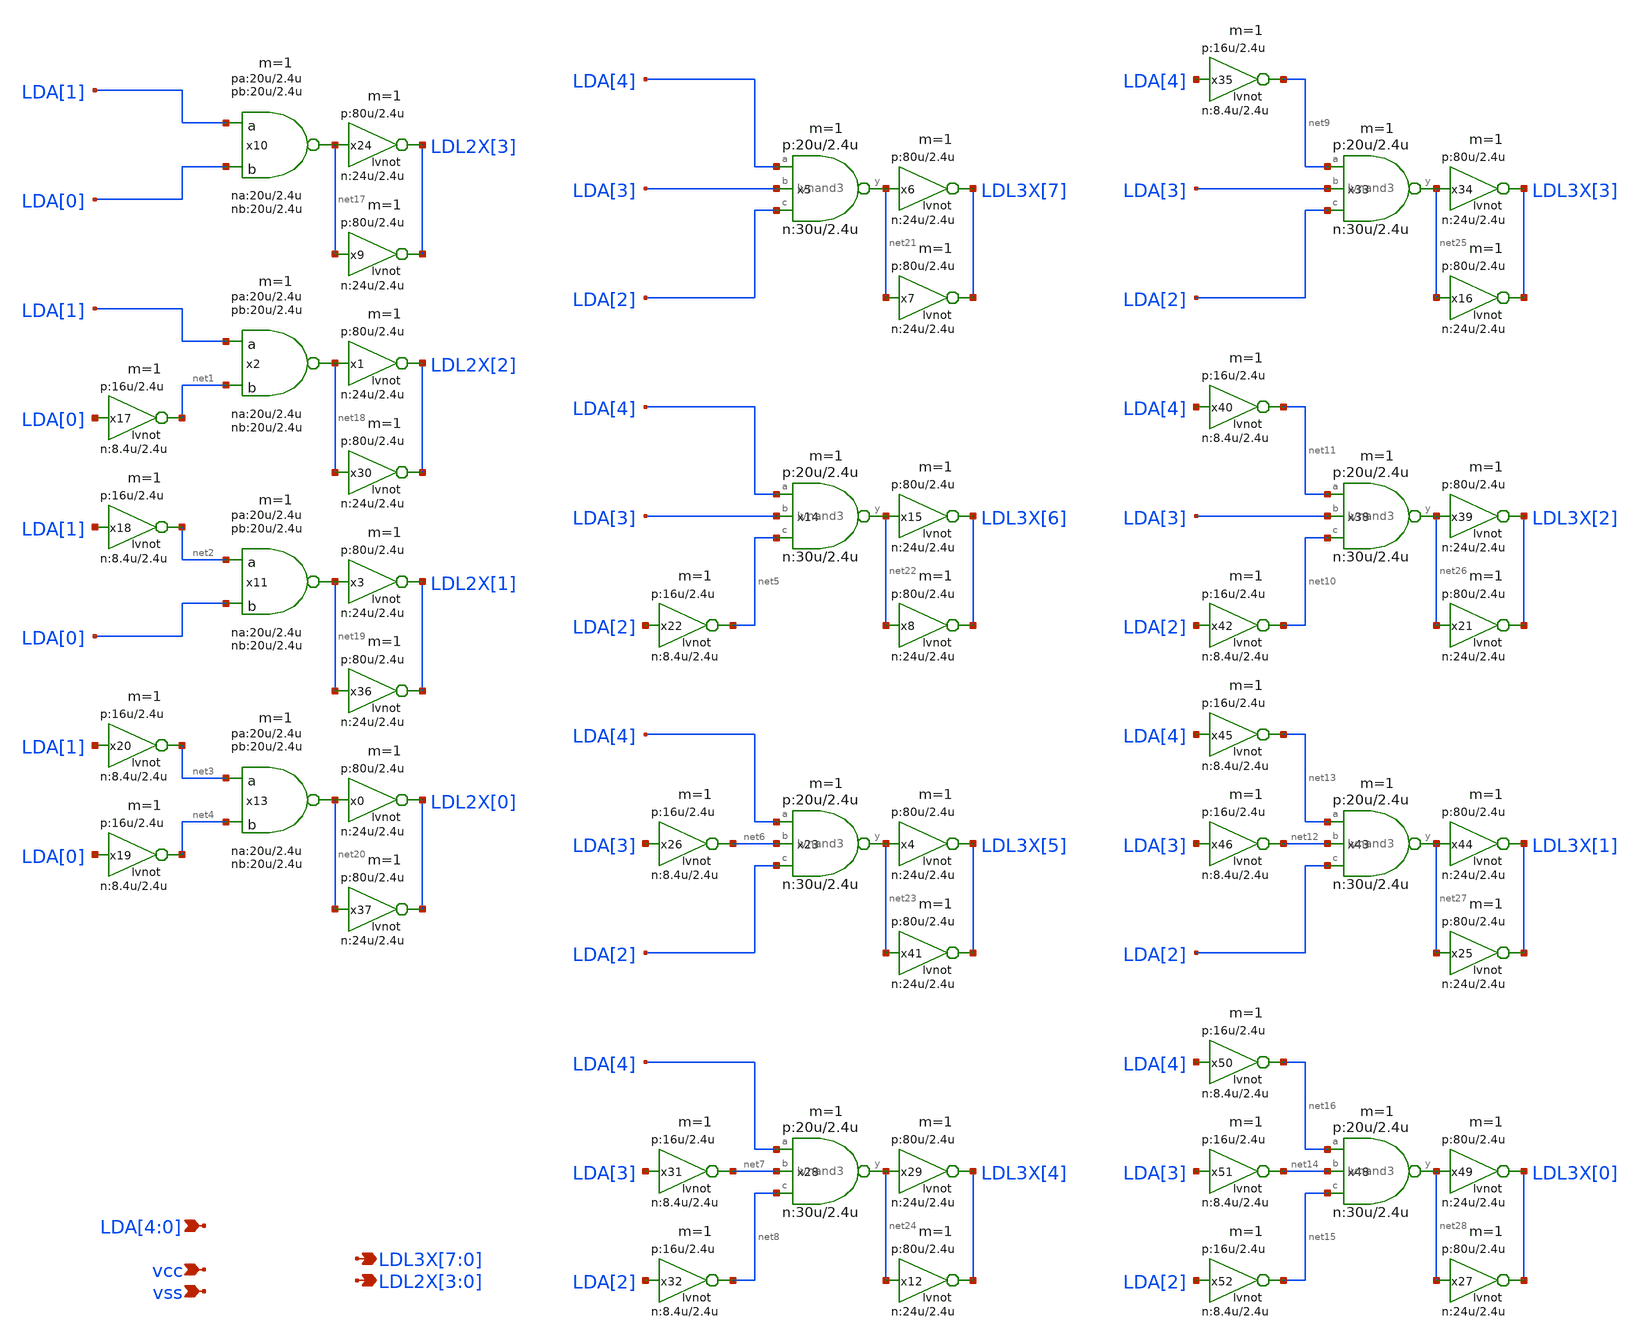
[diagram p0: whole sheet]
** sch_path: xschem-src/xschem_library/rom8k/rom2_predec4.sch
* Copyright (C) 1998-2026 Stefan Frederik Schippers
* This program is free software; you can redistribute it and/or modify
* it under the terms of the GNU General Public License as published by
* the Free Software Foundation; either version 2 of the License, or
* (at your option) any later version.
* This program is distributed in the hope that it will be useful,
* but WITHOUT ANY WARRANTY; without even the implied warranty of
* MERCHANTABILITY or FITNESS FOR A PARTICULAR PURPOSE.  See the
* GNU General Public License for more details.
* You should have received a copy of the GNU General Public License
* along with this program; if not, write to the Free Software
**.subckt rom2_predec4 LDA[4],LDA[3],LDA[2],LDA[1],LDA[0] vcc vss
*+ LDL2X[3],LDL2X[2],LDL2X[1],LDL2X[0] LDL3X[7],LDL3X[6],LDL3X[5],LDL3X[4],LDL3X[3],LDL3X[2],LDL3X[1],LDL3X[0]
*.ipin LDA[4],LDA[3],LDA[2],LDA[1],LDA[0]
*.ipin vcc
*.ipin vss
*.opin LDL2X[3],LDL2X[2],LDL2X[1],LDL2X[0]
*.opin LDL3X[7],LDL3X[6],LDL3X[5],LDL3X[4],LDL3X[3],LDL3X[2],LDL3X[1],LDL3X[0]
x10 net17 LDA[1] LDA[0] vcc vss lvnand2 wna=20u lna=2.4u wpa=20u lpa=2.4u wnb=20u lnb=2.4u wpb=20u
+ lpb=2.4u m=1
x2 net18 LDA[1] net1 vcc vss lvnand2 wna=20u lna=2.4u wpa=20u lpa=2.4u wnb=20u lnb=2.4u wpb=20u
+ lpb=2.4u m=1
x11 net19 net2 LDA[0] vcc vss lvnand2 wna=20u lna=2.4u wpa=20u lpa=2.4u wnb=20u lnb=2.4u wpb=20u
+ lpb=2.4u m=1
x13 net20 net3 net4 vcc vss lvnand2 wna=20u lna=2.4u wpa=20u lpa=2.4u wnb=20u lnb=2.4u wpb=20u
+ lpb=2.4u m=1
x17 net1 LDA[0] vcc vss lvnot wn=8.4u lln=2.4u wp=16u lp=2.4u m=1
x18 net2 LDA[1] vcc vss lvnot wn=8.4u lln=2.4u wp=16u lp=2.4u m=1
x19 net4 LDA[0] vcc vss lvnot wn=8.4u lln=2.4u wp=16u lp=2.4u m=1
x20 net3 LDA[1] vcc vss lvnot wn=8.4u lln=2.4u wp=16u lp=2.4u m=1
x5 net21 LDA[4] LDA[3] LDA[2] vcc vss lvnand3 wn=30u lln=2.4u wp=20u lp=2.4u m=1
x6 LDL3X[7] net21 vcc vss lvnot wn=24u lln=2.4u wp=80u lp=2.4u m=1
x14 net22 LDA[4] LDA[3] net5 vcc vss lvnand3 wn=30u lln=2.4u wp=20u lp=2.4u m=1
x15 LDL3X[6] net22 vcc vss lvnot wn=24u lln=2.4u wp=80u lp=2.4u m=1
x22 net5 LDA[2] vcc vss lvnot wn=8.4u lln=2.4u wp=16u lp=2.4u m=1
x23 net23 LDA[4] net6 LDA[2] vcc vss lvnand3 wn=30u lln=2.4u wp=20u lp=2.4u m=1
x24 LDL2X[3] net17 vcc vss lvnot wn=24u lln=2.4u wp=80u lp=2.4u m=1
x26 net6 LDA[3] vcc vss lvnot wn=8.4u lln=2.4u wp=16u lp=2.4u m=1
x28 net24 LDA[4] net7 net8 vcc vss lvnand3 wn=30u lln=2.4u wp=20u lp=2.4u m=1
x29 LDL3X[4] net24 vcc vss lvnot wn=24u lln=2.4u wp=80u lp=2.4u m=1
x31 net7 LDA[3] vcc vss lvnot wn=8.4u lln=2.4u wp=16u lp=2.4u m=1
x32 net8 LDA[2] vcc vss lvnot wn=8.4u lln=2.4u wp=16u lp=2.4u m=1
x33 net25 net9 LDA[3] LDA[2] vcc vss lvnand3 wn=30u lln=2.4u wp=20u lp=2.4u m=1
x34 LDL3X[3] net25 vcc vss lvnot wn=24u lln=2.4u wp=80u lp=2.4u m=1
x35 net9 LDA[4] vcc vss lvnot wn=8.4u lln=2.4u wp=16u lp=2.4u m=1
x38 net26 net11 LDA[3] net10 vcc vss lvnand3 wn=30u lln=2.4u wp=20u lp=2.4u m=1
x39 LDL3X[2] net26 vcc vss lvnot wn=24u lln=2.4u wp=80u lp=2.4u m=1
x40 net11 LDA[4] vcc vss lvnot wn=8.4u lln=2.4u wp=16u lp=2.4u m=1
x42 net10 LDA[2] vcc vss lvnot wn=8.4u lln=2.4u wp=16u lp=2.4u m=1
x43 net27 net13 net12 LDA[2] vcc vss lvnand3 wn=30u lln=2.4u wp=20u lp=2.4u m=1
x44 LDL3X[1] net27 vcc vss lvnot wn=24u lln=2.4u wp=80u lp=2.4u m=1
x45 net13 LDA[4] vcc vss lvnot wn=8.4u lln=2.4u wp=16u lp=2.4u m=1
x46 net12 LDA[3] vcc vss lvnot wn=8.4u lln=2.4u wp=16u lp=2.4u m=1
x48 net28 net16 net14 net15 vcc vss lvnand3 wn=30u lln=2.4u wp=20u lp=2.4u m=1
x49 LDL3X[0] net28 vcc vss lvnot wn=24u lln=2.4u wp=80u lp=2.4u m=1
x50 net16 LDA[4] vcc vss lvnot wn=8.4u lln=2.4u wp=16u lp=2.4u m=1
x51 net14 LDA[3] vcc vss lvnot wn=8.4u lln=2.4u wp=16u lp=2.4u m=1
x52 net15 LDA[2] vcc vss lvnot wn=8.4u lln=2.4u wp=16u lp=2.4u m=1
x1 LDL2X[2] net18 vcc vss lvnot wn=24u lln=2.4u wp=80u lp=2.4u m=1
x3 LDL2X[1] net19 vcc vss lvnot wn=24u lln=2.4u wp=80u lp=2.4u m=1
x0 LDL2X[0] net20 vcc vss lvnot wn=24u lln=2.4u wp=80u lp=2.4u m=1
x4 LDL3X[5] net23 vcc vss lvnot wn=24u lln=2.4u wp=80u lp=2.4u m=1
x7 LDL3X[7] net21 vcc vss lvnot wn=24u lln=2.4u wp=80u lp=2.4u m=1
x8 LDL3X[6] net22 vcc vss lvnot wn=24u lln=2.4u wp=80u lp=2.4u m=1
x9 LDL2X[3] net17 vcc vss lvnot wn=24u lln=2.4u wp=80u lp=2.4u m=1
x12 LDL3X[4] net24 vcc vss lvnot wn=24u lln=2.4u wp=80u lp=2.4u m=1
x16 LDL3X[3] net25 vcc vss lvnot wn=24u lln=2.4u wp=80u lp=2.4u m=1
x21 LDL3X[2] net26 vcc vss lvnot wn=24u lln=2.4u wp=80u lp=2.4u m=1
x25 LDL3X[1] net27 vcc vss lvnot wn=24u lln=2.4u wp=80u lp=2.4u m=1
x27 LDL3X[0] net28 vcc vss lvnot wn=24u lln=2.4u wp=80u lp=2.4u m=1
x30 LDL2X[2] net18 vcc vss lvnot wn=24u lln=2.4u wp=80u lp=2.4u m=1
x36 LDL2X[1] net19 vcc vss lvnot wn=24u lln=2.4u wp=80u lp=2.4u m=1
x37 LDL2X[0] net20 vcc vss lvnot wn=24u lln=2.4u wp=80u lp=2.4u m=1
x41 LDL3X[5] net23 vcc vss lvnot wn=24u lln=2.4u wp=80u lp=2.4u m=1
**.ends

* expanding   symbol:  lvnand2.sym # of pins=3
** sym_path: xschem-src/xschem_library/rom8k/lvnand2.sym
** sch_path: xschem-src/xschem_library/rom8k/lvnand2.sch
.subckt lvnand2 y a b VCCPIN VSSPIN     wna=8u lna=1.2u wpa=10u lpa=1.2u  wnb=8u lnb=1.2u wpb=10u
+ lpb=1.2u
*.opin y
*.ipin a
*.ipin b
m2 y a VCCPIN VCCPIN cmosp w=wpa l=lpa ad='wpa *4.6u' as='wpa *4.6u' pd='wpa *2+9.2u' ps='wpa *2+9.2u'
+ m=1
m1 y b VCCPIN VCCPIN cmosp w=wpb l=lpb ad='wpb *4.6u' as='wpb *4.6u' pd='wpb *2+9.2u' ps='wpb *2+9.2u'
+ m=1
m3 y a net1 VSSPIN cmosn w=wna l=lna ad='wna *4.3u' as='wna *4.3u' pd='wna *2+8.6u' ps='wna *2+8.6u'
+ m=1
m4 net1 b VSSPIN VSSPIN cmosn w=wnb l=lnb ad='wnb *4.3u' as='wnb *4.3u' pd='wnb *2+8.6u' ps='wnb *2+8.6u'
+ m=1
.ends


* expanding   symbol:  lvnot.sym # of pins=2
** sym_path: xschem-src/xschem_library/rom8k/lvnot.sym
** sch_path: xschem-src/xschem_library/rom8k/lvnot.sch
.subckt lvnot y a VCCPIN VSSPIN     wn=10u lln=1.2u wp=10u lp=1.2u
*.opin y
*.ipin a
m2 DP a VCCPIN VCCPIN cmosp w=wp l=lp ad='wp *4.6u' as='wp *4.6u' pd='wp *2+9.2u' ps='wp *2+9.2u' m=1
m1 DN a VSSPIN VSSPIN cmosn w=wn l=lln ad='wn *4.3u' as='wn *4.3u' pd='wn *2+8.6u' ps='wn *2+8.6u' m=1
Vmeas DP y 0
.save i(vmeas)
Vmeas1 y DN 0
.save i(vmeas1)
.save v(dp)
.save v(dn)
.ends


* expanding   symbol:  lvnand3.sym # of pins=4
** sym_path: xschem-src/xschem_library/rom8k/lvnand3.sym
** sch_path: xschem-src/xschem_library/rom8k/lvnand3.sch
.subckt lvnand3 y a b c VCCPIN VSSPIN     wn=18u lln=1.2u wp=10u lp=1.2u
*.opin y
*.ipin a
*.ipin b
*.ipin c
m1 net2 a VSSPIN VSSPIN cmosn w=wn l=lln ad={wn *2.2u} as={wn *2.2u} pd={wn *2+4.4u} ps={wn *2+4.4u}
+ m=1
m2 y a VCCPIN VCCPIN cmosp w=wp l=lp ad={wp *2.2u} as={wp *2.2u} pd={wp *2+4.4u} ps={wp *2+4.4u} m=1
m3 y b VCCPIN VCCPIN cmosp w=wp l=lp ad={wp *2.2u} as={wp *2.2u} pd={wp *2+4.4u} ps={wp *2+4.4u} m=1
m5 y c net1 VSSPIN cmosn w=wn l=lln ad={wn *2.2u} as={wn *2.2u} pd={wn *2+4.4u} ps={wn *2+4.4u} m=1
m4 y c VCCPIN VCCPIN cmosp w=wp l=lp ad={wp *2.2u} as={wp *2.2u} pd={wp *2+4.4u} ps={wp *2+4.4u} m=1
m6 net1 b net2 VSSPIN cmosn w=wn l=lln ad={wn *2.2u} as={wn *2.2u} pd={wn *2+4.4u} ps={wn *2+4.4u} m=1
.ends

.end
